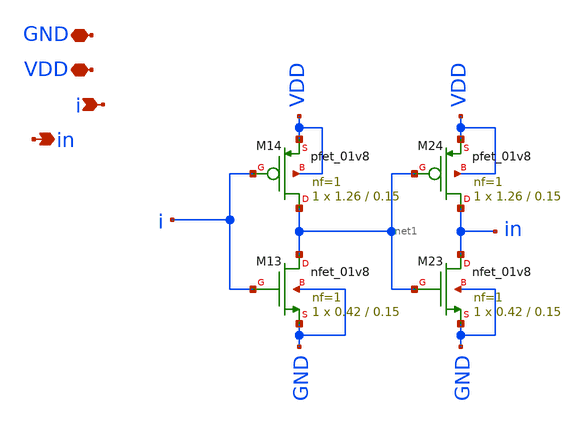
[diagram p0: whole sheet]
** sch_path: xschem/charge_pumps2/buffer_digital.sch
**.subckt buffer_digital i VDD GND in
*.ipin i
*.iopin VDD
*.iopin GND
*.opin in
XM13 net1 i GND GND sky130_fd_pr__nfet_01v8 L=0.15 W=0.42 nf=1 ad='int((nf+1)/2) * W/nf * 0.29' as='int((nf+2)/2) * W/nf * 0.29'
+ pd='2*int((nf+1)/2) * (W/nf + 0.29)' ps='2*int((nf+2)/2) * (W/nf + 0.29)' nrd='0.29 / W' nrs='0.29 / W'
+ sa=0 sb=0 sd=0 mult=1 m=1
XM14 net1 i VDD VDD sky130_fd_pr__pfet_01v8 L=0.15 W=1.26 nf=1 ad='int((nf+1)/2) * W/nf * 0.29' as='int((nf+2)/2) * W/nf * 0.29'
+ pd='2*int((nf+1)/2) * (W/nf + 0.29)' ps='2*int((nf+2)/2) * (W/nf + 0.29)' nrd='0.29 / W' nrs='0.29 / W'
+ sa=0 sb=0 sd=0 mult=1 m=1
XM23 in net1 GND GND sky130_fd_pr__nfet_01v8 L=0.15 W=0.42 nf=1 ad='int((nf+1)/2) * W/nf * 0.29' as='int((nf+2)/2) * W/nf * 0.29'
+ pd='2*int((nf+1)/2) * (W/nf + 0.29)' ps='2*int((nf+2)/2) * (W/nf + 0.29)' nrd='0.29 / W' nrs='0.29 / W'
+ sa=0 sb=0 sd=0 mult=1 m=1
XM24 in net1 VDD VDD sky130_fd_pr__pfet_01v8 L=0.15 W=1.26 nf=1 ad='int((nf+1)/2) * W/nf * 0.29' as='int((nf+2)/2) * W/nf * 0.29'
+ pd='2*int((nf+1)/2) * (W/nf + 0.29)' ps='2*int((nf+2)/2) * (W/nf + 0.29)' nrd='0.29 / W' nrs='0.29 / W'
+ sa=0 sb=0 sd=0 mult=1 m=1
**.ends
.end
